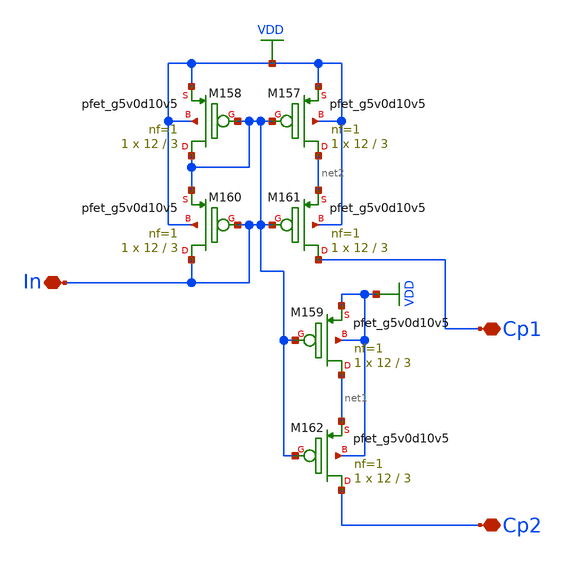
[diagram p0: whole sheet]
** sch_path: xschem/untitled-5.sch
**.subckt untitled-5 In Cp1 Cp2
*.iopin In
*.iopin Cp1
*.iopin Cp2
XM157 net2 In VDD VDD sky130_fd_pr__pfet_g5v0d10v5 L=3 W=12 nf=1 ad='int((nf+1)/2) * W/nf * 0.29' as='int((nf+2)/2) * W/nf * 0.29'
+ pd='2*int((nf+1)/2) * (W/nf + 0.29)' ps='2*int((nf+2)/2) * (W/nf + 0.29)' nrd='0.29 / W' nrs='0.29 / W'
+ sa=0 sb=0 sd=0 mult=1 m=1
XM158 In In VDD VDD sky130_fd_pr__pfet_g5v0d10v5 L=3 W=12 nf=1 ad='int((nf+1)/2) * W/nf * 0.29' as='int((nf+2)/2) * W/nf * 0.29'
+ pd='2*int((nf+1)/2) * (W/nf + 0.29)' ps='2*int((nf+2)/2) * (W/nf + 0.29)' nrd='0.29 / W' nrs='0.29 / W'
+ sa=0 sb=0 sd=0 mult=1 m=1
XM159 net1 In VDD VDD sky130_fd_pr__pfet_g5v0d10v5 L=3 W=12 nf=1 ad='int((nf+1)/2) * W/nf * 0.29' as='int((nf+2)/2) * W/nf * 0.29'
+ pd='2*int((nf+1)/2) * (W/nf + 0.29)' ps='2*int((nf+2)/2) * (W/nf + 0.29)' nrd='0.29 / W' nrs='0.29 / W'
+ sa=0 sb=0 sd=0 mult=1 m=1
XM160 In In In VDD sky130_fd_pr__pfet_g5v0d10v5 L=3 W=12 nf=1 ad='int((nf+1)/2) * W/nf * 0.29' as='int((nf+2)/2) * W/nf * 0.29'
+ pd='2*int((nf+1)/2) * (W/nf + 0.29)' ps='2*int((nf+2)/2) * (W/nf + 0.29)' nrd='0.29 / W' nrs='0.29 / W'
+ sa=0 sb=0 sd=0 mult=1 m=1
XM161 Cp1 In net2 VDD sky130_fd_pr__pfet_g5v0d10v5 L=3 W=12 nf=1 ad='int((nf+1)/2) * W/nf * 0.29' as='int((nf+2)/2) * W/nf * 0.29'
+ pd='2*int((nf+1)/2) * (W/nf + 0.29)' ps='2*int((nf+2)/2) * (W/nf + 0.29)' nrd='0.29 / W' nrs='0.29 / W'
+ sa=0 sb=0 sd=0 mult=1 m=1
XM162 Cp2 In net1 VDD sky130_fd_pr__pfet_g5v0d10v5 L=3 W=12 nf=1 ad='int((nf+1)/2) * W/nf * 0.29' as='int((nf+2)/2) * W/nf * 0.29'
+ pd='2*int((nf+1)/2) * (W/nf + 0.29)' ps='2*int((nf+2)/2) * (W/nf + 0.29)' nrd='0.29 / W' nrs='0.29 / W'
+ sa=0 sb=0 sd=0 mult=1 m=1
**.ends
.GLOBAL VDD
.end
